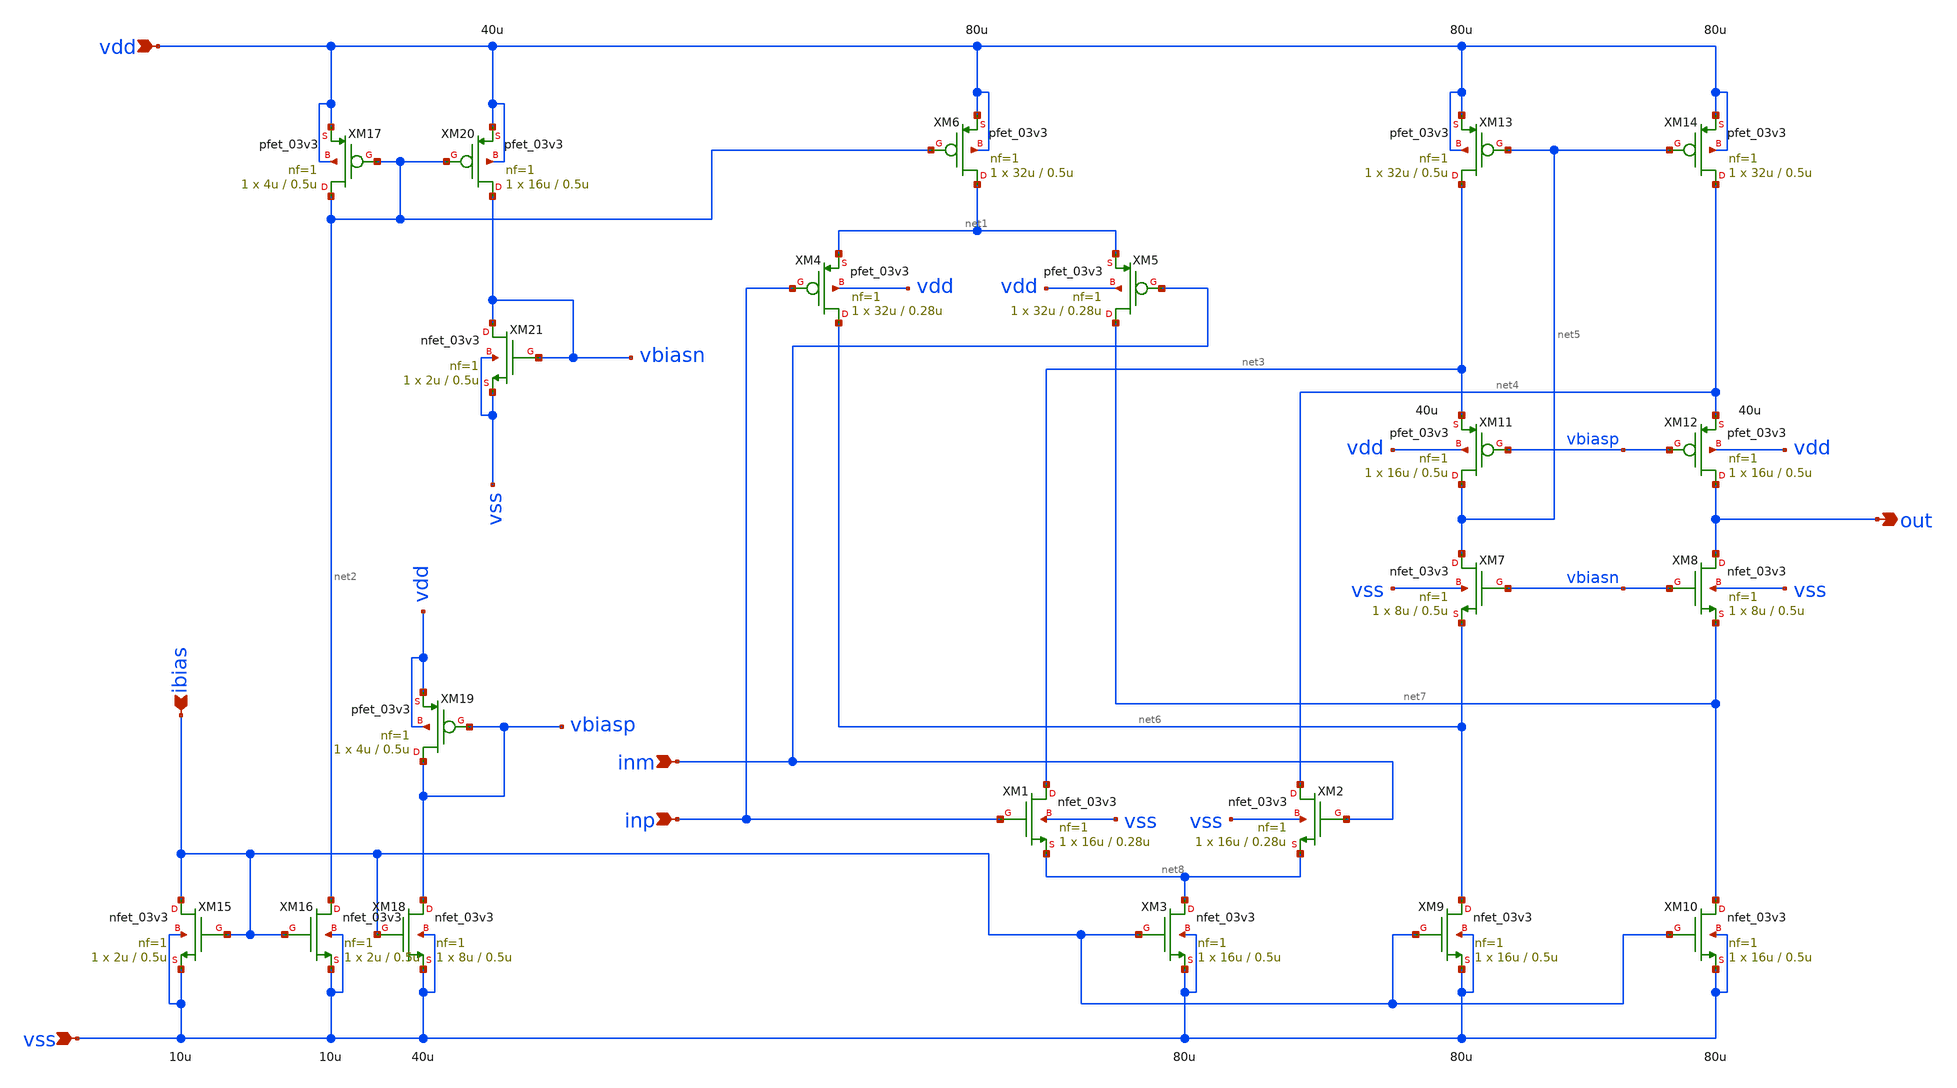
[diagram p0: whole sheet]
** sch_path: xschem/r2r_opamp.sch
**.subckt r2r_opamp vss vdd ibias inp inm out
*.ipin vss
*.ipin vdd
*.ipin ibias
*.ipin inp
*.ipin inm
*.opin out
XM1 net3 inp net8 vss nfet_03v3 L=0.28u W=16u nf=1 ad='int((nf+1)/2) * W/nf * 0.18u' as='int((nf+2)/2) * W/nf * 0.18u'
+ pd='2*int((nf+1)/2) * (W/nf + 0.18u)' ps='2*int((nf+2)/2) * (W/nf + 0.18u)' nrd='0.18u / W' nrs='0.18u / W'
+ sa=0 sb=0 sd=0 m=1
XM2 net4 inm net8 vss nfet_03v3 L=0.28u W=16u nf=1 ad='int((nf+1)/2) * W/nf * 0.18u' as='int((nf+2)/2) * W/nf * 0.18u'
+ pd='2*int((nf+1)/2) * (W/nf + 0.18u)' ps='2*int((nf+2)/2) * (W/nf + 0.18u)' nrd='0.18u / W' nrs='0.18u / W'
+ sa=0 sb=0 sd=0 m=1
XM3 net8 ibias vss vss nfet_03v3 L=0.5u W=16u nf=1 ad='int((nf+1)/2) * W/nf * 0.18u' as='int((nf+2)/2) * W/nf * 0.18u'
+ pd='2*int((nf+1)/2) * (W/nf + 0.18u)' ps='2*int((nf+2)/2) * (W/nf + 0.18u)' nrd='0.18u / W' nrs='0.18u / W'
+ sa=0 sb=0 sd=0 m=1
XM4 net6 inp net1 vdd pfet_03v3 L=0.28u W=32u nf=1 ad='int((nf+1)/2) * W/nf * 0.18u' as='int((nf+2)/2) * W/nf * 0.18u'
+ pd='2*int((nf+1)/2) * (W/nf + 0.18u)' ps='2*int((nf+2)/2) * (W/nf + 0.18u)' nrd='0.18u / W' nrs='0.18u / W'
+ sa=0 sb=0 sd=0 m=1
XM5 net7 inm net1 vdd pfet_03v3 L=0.28u W=32u nf=1 ad='int((nf+1)/2) * W/nf * 0.18u' as='int((nf+2)/2) * W/nf * 0.18u'
+ pd='2*int((nf+1)/2) * (W/nf + 0.18u)' ps='2*int((nf+2)/2) * (W/nf + 0.18u)' nrd='0.18u / W' nrs='0.18u / W'
+ sa=0 sb=0 sd=0 m=1
XM6 net1 net2 vdd vdd pfet_03v3 L=0.5u W=32u nf=1 ad='int((nf+1)/2) * W/nf * 0.18u' as='int((nf+2)/2) * W/nf * 0.18u'
+ pd='2*int((nf+1)/2) * (W/nf + 0.18u)' ps='2*int((nf+2)/2) * (W/nf + 0.18u)' nrd='0.18u / W' nrs='0.18u / W'
+ sa=0 sb=0 sd=0 m=1
XM7 net5 vbiasn net6 vss nfet_03v3 L=0.5u W=8u nf=1 ad='int((nf+1)/2) * W/nf * 0.18u' as='int((nf+2)/2) * W/nf * 0.18u'
+ pd='2*int((nf+1)/2) * (W/nf + 0.18u)' ps='2*int((nf+2)/2) * (W/nf + 0.18u)' nrd='0.18u / W' nrs='0.18u / W'
+ sa=0 sb=0 sd=0 m=1
XM8 out vbiasn net7 vss nfet_03v3 L=0.5u W=8u nf=1 ad='int((nf+1)/2) * W/nf * 0.18u' as='int((nf+2)/2) * W/nf * 0.18u'
+ pd='2*int((nf+1)/2) * (W/nf + 0.18u)' ps='2*int((nf+2)/2) * (W/nf + 0.18u)' nrd='0.18u / W' nrs='0.18u / W'
+ sa=0 sb=0 sd=0 m=1
XM9 net6 ibias vss vss nfet_03v3 L=0.5u W=16u nf=1 ad='int((nf+1)/2) * W/nf * 0.18u' as='int((nf+2)/2) * W/nf * 0.18u'
+ pd='2*int((nf+1)/2) * (W/nf + 0.18u)' ps='2*int((nf+2)/2) * (W/nf + 0.18u)' nrd='0.18u / W' nrs='0.18u / W'
+ sa=0 sb=0 sd=0 m=1
XM10 net7 ibias vss vss nfet_03v3 L=0.5u W=16u nf=1 ad='int((nf+1)/2) * W/nf * 0.18u' as='int((nf+2)/2) * W/nf * 0.18u'
+ pd='2*int((nf+1)/2) * (W/nf + 0.18u)' ps='2*int((nf+2)/2) * (W/nf + 0.18u)' nrd='0.18u / W' nrs='0.18u / W'
+ sa=0 sb=0 sd=0 m=1
XM11 net5 vbiasp net3 vdd pfet_03v3 L=0.5u W=16u nf=1 ad='int((nf+1)/2) * W/nf * 0.18u' as='int((nf+2)/2) * W/nf * 0.18u'
+ pd='2*int((nf+1)/2) * (W/nf + 0.18u)' ps='2*int((nf+2)/2) * (W/nf + 0.18u)' nrd='0.18u / W' nrs='0.18u / W'
+ sa=0 sb=0 sd=0 m=1
XM12 out vbiasp net4 vdd pfet_03v3 L=0.5u W=16u nf=1 ad='int((nf+1)/2) * W/nf * 0.18u' as='int((nf+2)/2) * W/nf * 0.18u'
+ pd='2*int((nf+1)/2) * (W/nf + 0.18u)' ps='2*int((nf+2)/2) * (W/nf + 0.18u)' nrd='0.18u / W' nrs='0.18u / W'
+ sa=0 sb=0 sd=0 m=1
XM13 net3 net5 vdd vdd pfet_03v3 L=0.5u W=32u nf=1 ad='int((nf+1)/2) * W/nf * 0.18u' as='int((nf+2)/2) * W/nf * 0.18u'
+ pd='2*int((nf+1)/2) * (W/nf + 0.18u)' ps='2*int((nf+2)/2) * (W/nf + 0.18u)' nrd='0.18u / W' nrs='0.18u / W'
+ sa=0 sb=0 sd=0 m=1
XM14 net4 net5 vdd vdd pfet_03v3 L=0.5u W=32u nf=1 ad='int((nf+1)/2) * W/nf * 0.18u' as='int((nf+2)/2) * W/nf * 0.18u'
+ pd='2*int((nf+1)/2) * (W/nf + 0.18u)' ps='2*int((nf+2)/2) * (W/nf + 0.18u)' nrd='0.18u / W' nrs='0.18u / W'
+ sa=0 sb=0 sd=0 m=1
XM15 ibias ibias vss vss nfet_03v3 L=0.5u W=2u nf=1 ad='int((nf+1)/2) * W/nf * 0.18u' as='int((nf+2)/2) * W/nf * 0.18u'
+ pd='2*int((nf+1)/2) * (W/nf + 0.18u)' ps='2*int((nf+2)/2) * (W/nf + 0.18u)' nrd='0.18u / W' nrs='0.18u / W'
+ sa=0 sb=0 sd=0 m=1
XM16 net2 ibias vss vss nfet_03v3 L=0.5u W=2u nf=1 ad='int((nf+1)/2) * W/nf * 0.18u' as='int((nf+2)/2) * W/nf * 0.18u'
+ pd='2*int((nf+1)/2) * (W/nf + 0.18u)' ps='2*int((nf+2)/2) * (W/nf + 0.18u)' nrd='0.18u / W' nrs='0.18u / W'
+ sa=0 sb=0 sd=0 m=1
XM17 net2 net2 vdd vdd pfet_03v3 L=0.5u W=4u nf=1 ad='int((nf+1)/2) * W/nf * 0.18u' as='int((nf+2)/2) * W/nf * 0.18u'
+ pd='2*int((nf+1)/2) * (W/nf + 0.18u)' ps='2*int((nf+2)/2) * (W/nf + 0.18u)' nrd='0.18u / W' nrs='0.18u / W'
+ sa=0 sb=0 sd=0 m=1
XM18 vbiasp ibias vss vss nfet_03v3 L=0.5u W=8u nf=1 ad='int((nf+1)/2) * W/nf * 0.18u' as='int((nf+2)/2) * W/nf * 0.18u'
+ pd='2*int((nf+1)/2) * (W/nf + 0.18u)' ps='2*int((nf+2)/2) * (W/nf + 0.18u)' nrd='0.18u / W' nrs='0.18u / W'
+ sa=0 sb=0 sd=0 m=1
XM19 vbiasp vbiasp vdd vdd pfet_03v3 L=0.5u W=4u nf=1 ad='int((nf+1)/2) * W/nf * 0.18u' as='int((nf+2)/2) * W/nf * 0.18u'
+ pd='2*int((nf+1)/2) * (W/nf + 0.18u)' ps='2*int((nf+2)/2) * (W/nf + 0.18u)' nrd='0.18u / W' nrs='0.18u / W'
+ sa=0 sb=0 sd=0 m=1
XM20 vbiasn net2 vdd vdd pfet_03v3 L=0.5u W=16u nf=1 ad='int((nf+1)/2) * W/nf * 0.18u' as='int((nf+2)/2) * W/nf * 0.18u'
+ pd='2*int((nf+1)/2) * (W/nf + 0.18u)' ps='2*int((nf+2)/2) * (W/nf + 0.18u)' nrd='0.18u / W' nrs='0.18u / W'
+ sa=0 sb=0 sd=0 m=1
XM21 vbiasn vbiasn vss vss nfet_03v3 L=0.5u W=2u nf=1 ad='int((nf+1)/2) * W/nf * 0.18u' as='int((nf+2)/2) * W/nf * 0.18u'
+ pd='2*int((nf+1)/2) * (W/nf + 0.18u)' ps='2*int((nf+2)/2) * (W/nf + 0.18u)' nrd='0.18u / W' nrs='0.18u / W'
+ sa=0 sb=0 sd=0 m=1
**.ends
.end
